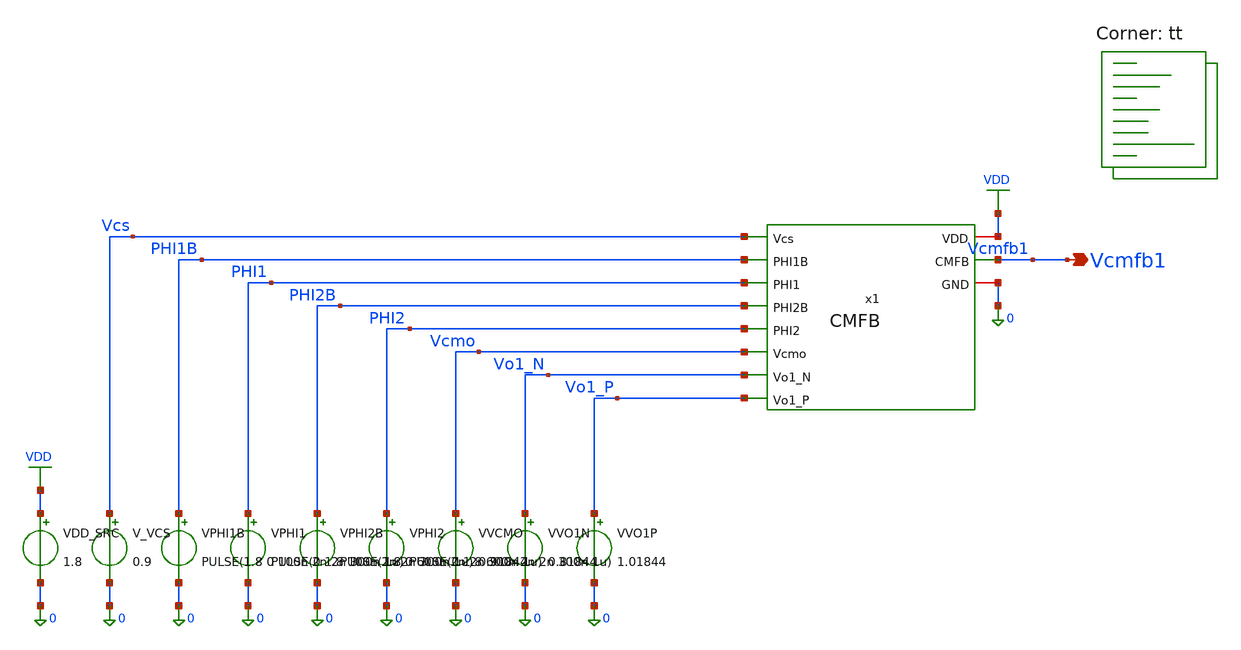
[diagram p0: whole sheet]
** sch_path: blocks/02_CMFB/sim/tb_CMFB.sch
**.subckt tb_CMFB Vcmfb1
*.opin Vcmfb1
x1 Vcmfb1 Vcs PHI1B PHI1 VDD PHI2B 0 PHI2 Vcmo Vo1_N Vo1_P CMFB
VDD_SRC VDD 0 1.8
V_VCS Vcs 0 0.9
VPHI1B PHI1B 0 PULSE(1.8 0 100n 2n 2n 300n 1u)
VPHI1 PHI1 0 PULSE(0 1.8 100n 2n 2n 300n 1u)
VPHI2B PHI2B 0 PULSE(1.8 0 600n 2n 2n 300n 1u)
VPHI2 PHI2 0 PULSE(0 1.8 600n 2n 2n 300n 1u)
VVCMO Vcmo 0 0.91844
VVO1N Vo1_N 0 0.81844
VVO1P Vo1_P 0 1.01844
**** begin user architecture code


* ============================================================
* SC-CMFB STANDALONE CHARACTERIZATION
* Differential-only test
*
* Expected source condition:
*   Vo1_P = 1.01844 V
*   Vo1_N = 0.81844 V
*
* Therefore:
*   V_OCM = (Vo1_P + Vo1_N)/2 = 0.91844 V
*   V_OD  = Vo1_P - Vo1_N     = 0.20000 V
*
* Expected:
*   Vcmfb1 average remains close to nominal ~0.9 V
* ============================================================

* Weak numerical DC path only
RLEAK Vcmfb1 0 1G

.control
save all

* ------------------------------------------------------------
* TRANSIENT
* ------------------------------------------------------------

tran 1n 10u uic


* ============================================================
* CLOCK CHECKS
* ============================================================

meas tran PHI1_MAX MAX v(phi1)
meas tran PHI1_MIN MIN v(phi1)

meas tran PHI1B_MAX MAX v(phi1b)
meas tran PHI1B_MIN MIN v(phi1b)

meas tran PHI2_MAX MAX v(phi2)
meas tran PHI2_MIN MIN v(phi2)

meas tran PHI2B_MAX MAX v(phi2b)
meas tran PHI2B_MIN MIN v(phi2b)


* ============================================================
* INPUT OUTPUT-COMMON-MODE CHECK
* Use final 2 us after settling
* ============================================================

meas tran VO1P_AVG AVG v(vo1_p) FROM=8u TO=10u
meas tran VO1N_AVG AVG v(vo1_n) FROM=8u TO=10u

let VOCM_INPUT = (VO1P_AVG + VO1N_AVG)/2
let VOD_INPUT  = VO1P_AVG - VO1N_AVG


* ============================================================
* VCMFB STEADY-STATE CHARACTERIZATION
* ============================================================

meas tran VCMFB_AVG AVG v(vcmfb1) FROM=8u TO=10u
meas tran VCMFB_MIN MIN v(vcmfb1) FROM=8u TO=10u
meas tran VCMFB_MAX MAX v(vcmfb1) FROM=8u TO=10u

let VCMFB_RIPPLE = VCMFB_MAX - VCMFB_MIN

* Reference control voltage used in testbench
let VCMFB_TARGET = 0.9

let VCMFB_DC_ERROR = VCMFB_AVG - VCMFB_TARGET
let VCMFB_DC_ERROR_ABS = abs(VCMFB_DC_ERROR)


* ============================================================
* PRINT RESULTS
* ============================================================

print PHI1_MAX
print PHI1_MIN
print PHI1B_MAX
print PHI1B_MIN

print PHI2_MAX
print PHI2_MIN
print PHI2B_MAX
print PHI2B_MIN

print VO1P_AVG
print VO1N_AVG
print VOCM_INPUT
print VOD_INPUT

print VCMFB_AVG
print VCMFB_MIN
print VCMFB_MAX
print VCMFB_RIPPLE

print VCMFB_TARGET
print VCMFB_DC_ERROR
print VCMFB_DC_ERROR_ABS


* ============================================================
* PLOTS
* ============================================================

plot v(phi1) v(phi2)
plot v(phi1b) v(phi2b)

plot v(vo1_p) v(vo1_n)

plot v(vcmfb1)

.endc


.lib $::SKYWATER_MODELS/sky130.lib.spice tt
**** end user architecture code
**.ends
.GLOBAL VDD
.end
